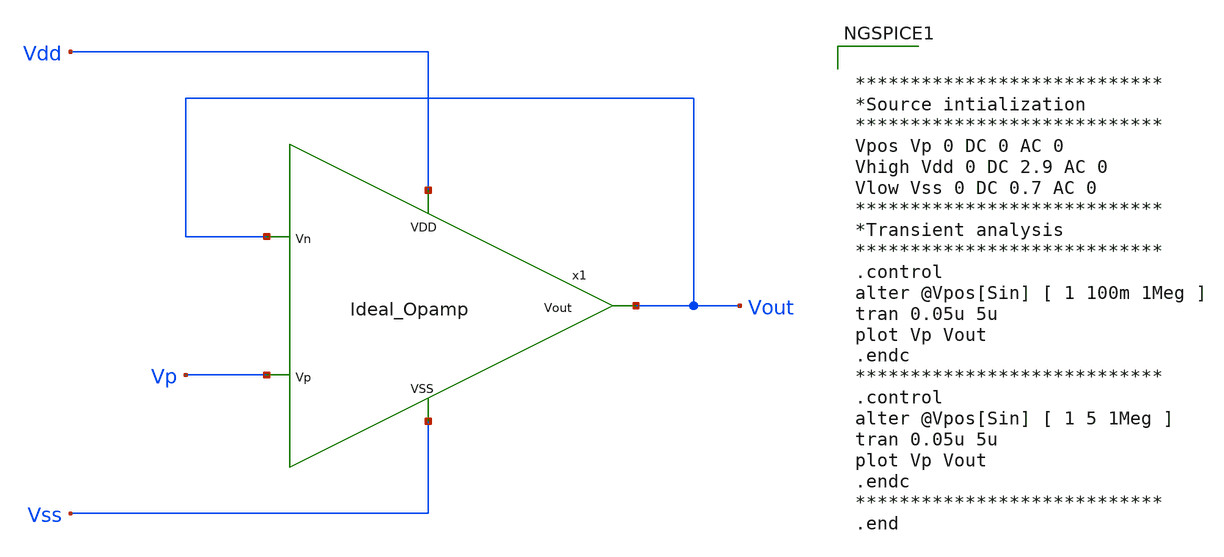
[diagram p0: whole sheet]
** sch_path: testing/test_Ideal_Opamp.sch
**.subckt test_Ideal_Opamp
x1 Vout Vp Vout Vss Vdd Ideal_Opamp
**** begin user architecture code


****************************
*Source intialization
****************************
Vpos Vp 0 DC 0 AC 0
Vhigh Vdd 0 DC 2.9 AC 0
Vlow Vss 0 DC 0.7 AC 0
****************************
*Transient analysis
****************************
.control
alter @Vpos[Sin] [ 1 100m 1Meg ]
tran 0.05u 5u
plot Vp Vout
.endc
****************************
.control
alter @Vpos[Sin] [ 1 5 1Meg ]
tran 0.05u 5u
plot Vp Vout
.endc
****************************
.end




.param mc_mm_switch=0
.param mc_pr_switch=0
.include ~/mabrains/Analog_blocks/models/sky130A/libs.ref/sky130_fd_pr/spice/sky130_fd_pr__nfet_01v8__tt.corner.spice
.include ~/mabrains/Analog_blocks/models/sky130A/libs.ref/sky130_fd_pr/spice/sky130_fd_pr__nfet_01v8_lvt__tt.corner.spice
.include ~/mabrains/Analog_blocks/models/sky130A/libs.ref/sky130_fd_pr/spice/sky130_fd_pr__pfet_01v8__tt.corner.spice
.include ~/mabrains/Analog_blocks/models/sky130A/libs.ref/sky130_fd_pr/spice/sky130_fd_pr__nfet_03v3_nvt__tt.corner.spice
.include ~/mabrains/Analog_blocks/models/sky130A/libs.ref/sky130_fd_pr/spice/sky130_fd_pr__nfet_05v0_nvt__tt.corner.spice
.include ~/mabrains/Analog_blocks/models/sky130A/libs.ref/sky130_fd_pr/spice/sky130_fd_pr__esd_nfet_01v8__tt.corner.spice
.include ~/mabrains/Analog_blocks/models/sky130A/libs.ref/sky130_fd_pr/spice/sky130_fd_pr__pfet_01v8_lvt__tt.corner.spice
.include ~/mabrains/Analog_blocks/models/sky130A/libs.ref/sky130_fd_pr/spice/sky130_fd_pr__pfet_01v8_hvt__tt.corner.spice
.include ~/mabrains/Analog_blocks/models/sky130A/libs.ref/sky130_fd_pr/spice/sky130_fd_pr__esd_pfet_g5v0d10v5__tt.corner.spice
.include ~/mabrains/Analog_blocks/models/sky130A/libs.ref/sky130_fd_pr/spice/sky130_fd_pr__pfet_g5v0d10v5__tt.corner.spice
.include ~/mabrains/Analog_blocks/models/sky130A/libs.ref/sky130_fd_pr/spice/sky130_fd_pr__pfet_g5v0d16v0__tt.corner.spice
.include ~/mabrains/Analog_blocks/models/sky130A/libs.ref/sky130_fd_pr/spice/sky130_fd_pr__nfet_g5v0d10v5__tt.corner.spice
.include ~/mabrains/Analog_blocks/models/sky130A/libs.ref/sky130_fd_pr/spice/sky130_fd_pr__nfet_g5v0d16v0__tt_discrete.corner.spice
.include ~/mabrains/Analog_blocks/models/sky130A/libs.ref/sky130_fd_pr/spice/sky130_fd_pr__esd_nfet_g5v0d10v5__tt.corner.spice
.include ~/mabrains/Analog_blocks/models/sky130A/libs.ref/sky130_fd_pr/spice/sky130_fd_pr__nfet_20v0__tt_discrete.corner.spice
.include ~/mabrains/Analog_blocks/models/sky130A/libs.ref/sky130_fd_pr/spice/sky130_fd_pr__pfet_20v0__tt_discrete.corner.spice
.include ~/mabrains/Analog_blocks/models/sky130A/libs.tech/ngspice/corners/tt/nonfet.spice
* Mismatch parameters
.include ~/mabrains/Analog_blocks/models/sky130A/libs.ref/sky130_fd_pr/spice/sky130_fd_pr__nfet_01v8__mismatch.corner.spice
.include ~/mabrains/Analog_blocks/models/sky130A/libs.ref/sky130_fd_pr/spice/sky130_fd_pr__pfet_01v8__mismatch.corner.spice
.include ~/mabrains/Analog_blocks/models/sky130A/libs.ref/sky130_fd_pr/spice/sky130_fd_pr__nfet_01v8_lvt__mismatch.corner.spice
.include ~/mabrains/Analog_blocks/models/sky130A/libs.ref/sky130_fd_pr/spice/sky130_fd_pr__pfet_01v8_lvt__mismatch.corner.spice
.include ~/mabrains/Analog_blocks/models/sky130A/libs.ref/sky130_fd_pr/spice/sky130_fd_pr__pfet_01v8_hvt__mismatch.corner.spice
.include ~/mabrains/Analog_blocks/models/sky130A/libs.ref/sky130_fd_pr/spice/sky130_fd_pr__nfet_g5v0d10v5__mismatch.corner.spice
.include ~/mabrains/Analog_blocks/models/sky130A/libs.ref/sky130_fd_pr/spice/sky130_fd_pr__pfet_g5v0d10v5__mismatch.corner.spice
.include ~/mabrains/Analog_blocks/models/sky130A/libs.ref/sky130_fd_pr/spice/sky130_fd_pr__nfet_05v0_nvt__mismatch.corner.spice
.include ~/mabrains/Analog_blocks/models/sky130A/libs.ref/sky130_fd_pr/spice/sky130_fd_pr__nfet_03v3_nvt__mismatch.corner.spice
* Resistor/Capacitor
.include ~/mabrains/Analog_blocks/models/sky130A/libs.tech/ngspice/r+c/res_typical__cap_typical.spice
.include ~/mabrains/Analog_blocks/models/sky130A/libs.tech/ngspice/r+c/res_typical__cap_typical__lin.spice
* Special cells
.include ~/mabrains/Analog_blocks/models/sky130A/libs.tech/ngspice/corners/tt/specialized_cells.spice
* All models
.include ~/mabrains/Analog_blocks/models/sky130A/libs.tech/ngspice/all.spice
* Corner
.include ~/mabrains/Analog_blocks/models/sky130A/libs.tech/ngspice/corners/tt/rf.spice



**** end user architecture code
**.ends

* expanding   symbol:  /home/eslam/mabrains/Analog_blocks/testing/Ideal_Opamp.sym # of pins=5
** sym_path: testing/Ideal_Opamp.sym
** sch_path: testing/Ideal_Opamp.sch
.subckt Ideal_Opamp Vout Vp Vn VSS VDD
*.ipin Vp
*.ipin Vn
*.opin Vout
*.ipin VDD
*.ipin VSS
E1 net1 0 Vp Vn 100000
R1 net1 Vout 100G m=1
XD1 Vout VDD sky130_fd_pr__diode_pw2nd_05v5 area=1 pj=4e6
XD2 VSS Vout sky130_fd_pr__diode_pw2nd_05v5 area=1 pj=4e6
.ends

.end
